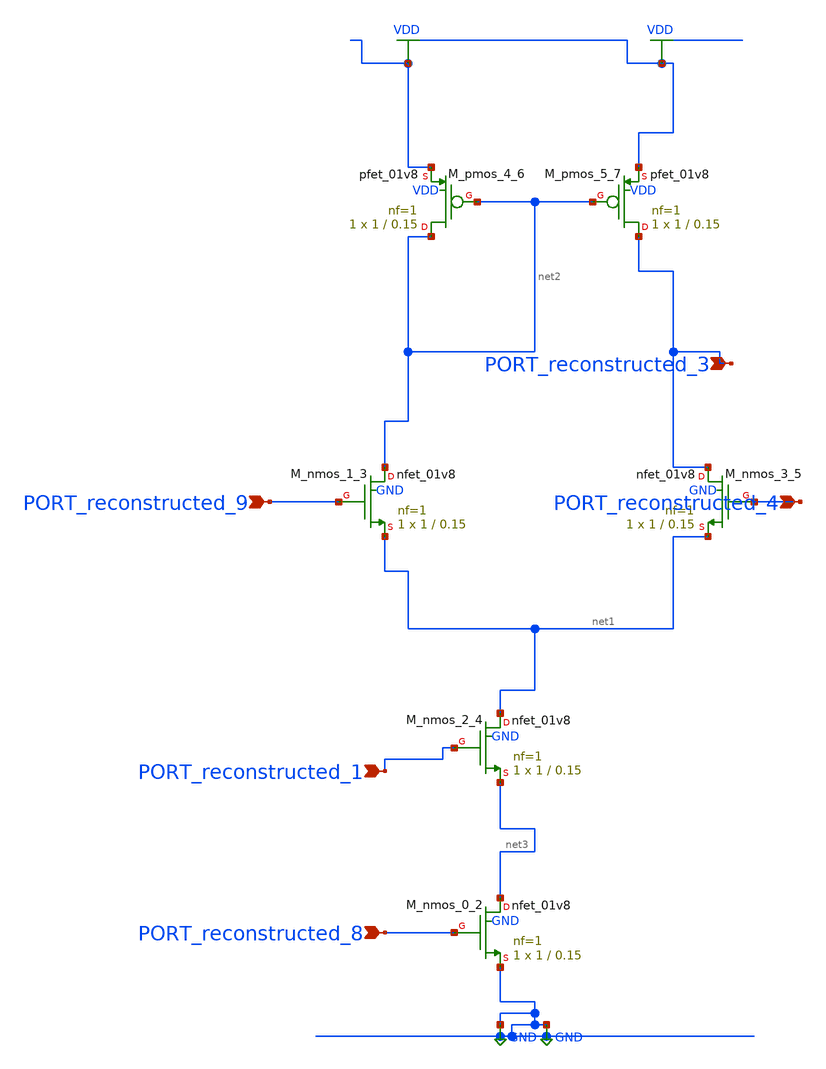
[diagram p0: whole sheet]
** sch_path: schematics/10_1587_elex_17_20200238_02_001_crop1.sch
**.subckt 10_1587_elex_17_20200238_02_001_crop1 PORT_reconstructed_4 PORT_reconstructed_8
*+ PORT_reconstructed_3 PORT_reconstructed_1 PORT_reconstructed_9
*.ipin PORT_reconstructed_4
*.ipin PORT_reconstructed_8
*.ipin PORT_reconstructed_3
*.ipin PORT_reconstructed_1
*.ipin PORT_reconstructed_9
XM_nmos_0_2 net3 PORT_reconstructed_8 GND GND sky130_fd_pr__nfet_01v8 L=0.15 W=1 nf=1 ad='int((1 + 1)/2) * 1 / 1 * 0.29'
+ as='int((1 + 2)/2) * 1 / 1 * 0.29' pd='2*int((1 + 1)/2) * (1 / 1 + 0.29)' ps='2*int((1 + 2)/2) * (1 / 1 + 0.29)'
+ nrd='0.29 / 1 ' nrs='0.29 / 1 ' sa=0 sb=0 sd=0 mult=1 m=1
XM_nmos_1_3 net2 PORT_reconstructed_9 net1 GND sky130_fd_pr__nfet_01v8 L=0.15 W=1 nf=1 ad='int((1 + 1)/2) * 1 / 1 * 0.29'
+ as='int((1 + 2)/2) * 1 / 1 * 0.29' pd='2*int((1 + 1)/2) * (1 / 1 + 0.29)' ps='2*int((1 + 2)/2) * (1 / 1 + 0.29)'
+ nrd='0.29 / 1 ' nrs='0.29 / 1 ' sa=0 sb=0 sd=0 mult=1 m=1
XM_nmos_2_4 net1 PORT_reconstructed_1 net3 GND sky130_fd_pr__nfet_01v8 L=0.15 W=1 nf=1 ad='int((1 + 1)/2) * 1 / 1 * 0.29'
+ as='int((1 + 2)/2) * 1 / 1 * 0.29' pd='2*int((1 + 1)/2) * (1 / 1 + 0.29)' ps='2*int((1 + 2)/2) * (1 / 1 + 0.29)'
+ nrd='0.29 / 1 ' nrs='0.29 / 1 ' sa=0 sb=0 sd=0 mult=1 m=1
XM_nmos_3_5 PORT_reconstructed_3 PORT_reconstructed_4 net1 GND sky130_fd_pr__nfet_01v8 L=0.15 W=1 nf=1
+ ad='int((1 + 1)/2) * 1 / 1 * 0.29' as='int((1 + 2)/2) * 1 / 1 * 0.29' pd='2*int((1 + 1)/2) * (1 / 1 + 0.29)'
+ ps='2*int((1 + 2)/2) * (1 / 1 + 0.29)' nrd='0.29 / 1 ' nrs='0.29 / 1 ' sa=0 sb=0 sd=0 mult=1 m=1
XM_pmos_4_6 net2 net2 VDD VDD sky130_fd_pr__pfet_01v8 L=0.15 W=1 nf=1 ad='int((1 + 1)/2) * 1 / 1 * 0.29'
+ as='int((1 + 2)/2) * 1 / 1 * 0.29' pd='2*int((1 + 1)/2) * (1 / 1 + 0.29)' ps='2*int((1 + 2)/2) * (1 / 1 + 0.29)'
+ nrd='0.29 / 1 ' nrs='0.29 / 1 ' sa=0 sb=0 sd=0 mult=1 m=1
XM_pmos_5_7 PORT_reconstructed_3 net2 VDD VDD sky130_fd_pr__pfet_01v8 L=0.15 W=1 nf=1 ad='int((1 + 1)/2) * 1 / 1 * 0.29'
+ as='int((1 + 2)/2) * 1 / 1 * 0.29' pd='2*int((1 + 1)/2) * (1 / 1 + 0.29)' ps='2*int((1 + 2)/2) * (1 / 1 + 0.29)'
+ nrd='0.29 / 1 ' nrs='0.29 / 1 ' sa=0 sb=0 sd=0 mult=1 m=1
**.ends
.GLOBAL GND
.GLOBAL VDD
.end
